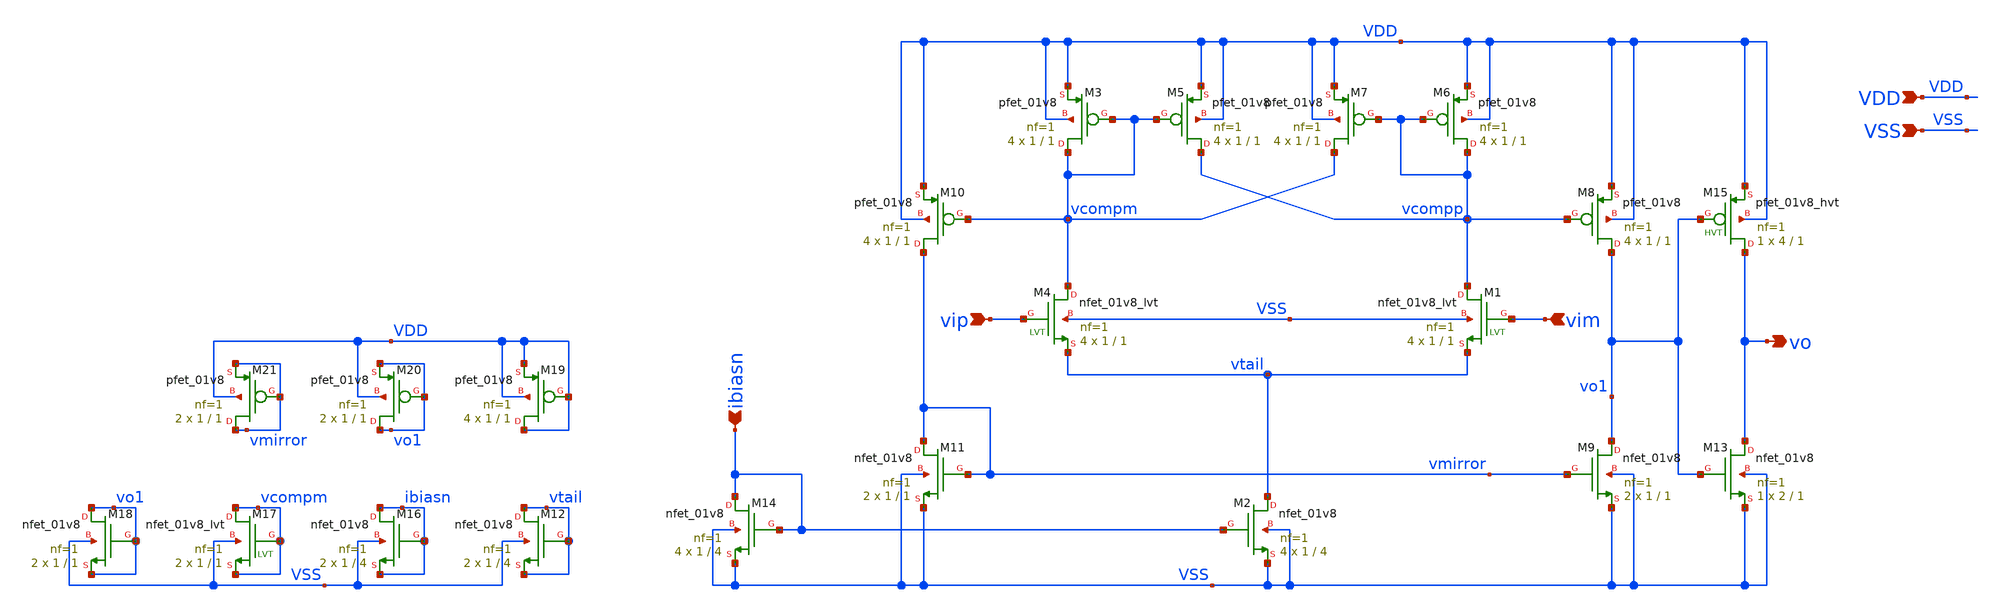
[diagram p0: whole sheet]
** sch_path: designs/comparator_lvs.sch
* Copyright 2020 Stefan Frederik Schippers
* Licensed under the Apache License, Version 2.0 (the "License");
* you may not use this file except in compliance with the License.
* You may obtain a copy of the License at
* https://www.apache.org/licenses/LICENSE-2.0
* Unless required by applicable law or agreed to in writing, software
* distributed under the License is distributed on an "AS IS" BASIS,
* WITHOUT WARRANTIES OR CONDITIONS OF ANY KIND, either express or implied.
* See the License for the specific language governing permissions and
* limitations under the License.
**.subckt comparator_lvs vip vim vo ibiasn VDD VSS
*.ipin vip
*.ipin vim
*.opin vo
*.ipin ibiasn
*.ipin VDD
*.ipin VSS
XM6 vcompp vcompp VDD VDD sky130_fd_pr__pfet_01v8 L=1 W=1 nf=1 ad='int((nf+1)/2) * W/nf * 0.29' as='int((nf+2)/2) * W/nf * 0.29'
+ pd='2*int((nf+1)/2) * (W/nf + 0.29)' ps='2*int((nf+2)/2) * (W/nf + 0.29)' nrd='0.29 / W' nrs='0.29 / W'
+ sa=0 sb=0 sd=0 mult=4 m=4
XM3 vcompm vcompm VDD VDD sky130_fd_pr__pfet_01v8 L=1 W=1 nf=1 ad='int((nf+1)/2) * W/nf * 0.29' as='int((nf+2)/2) * W/nf * 0.29'
+ pd='2*int((nf+1)/2) * (W/nf + 0.29)' ps='2*int((nf+2)/2) * (W/nf + 0.29)' nrd='0.29 / W' nrs='0.29 / W'
+ sa=0 sb=0 sd=0 mult=4 m=4
XM2 vtail ibiasn VSS VSS sky130_fd_pr__nfet_01v8 L=4 W=1 nf=1 ad='int((nf+1)/2) * W/nf * 0.29' as='int((nf+2)/2) * W/nf * 0.29'
+ pd='2*int((nf+1)/2) * (W/nf + 0.29)' ps='2*int((nf+2)/2) * (W/nf + 0.29)' nrd='0.29 / W' nrs='0.29 / W'
+ sa=0 sb=0 sd=0 mult=4 m=4
XM14 ibiasn ibiasn VSS VSS sky130_fd_pr__nfet_01v8 L=4 W=1 nf=1 ad='int((nf+1)/2) * W/nf * 0.29' as='int((nf+2)/2) * W/nf * 0.29'
+ pd='2*int((nf+1)/2) * (W/nf + 0.29)' ps='2*int((nf+2)/2) * (W/nf + 0.29)' nrd='0.29 / W' nrs='0.29 / W'
+ sa=0 sb=0 sd=0 mult=4 m=4
XM4 vcompm vip vtail VSS sky130_fd_pr__nfet_01v8_lvt L=1 W=1 nf=1 ad='int((nf+1)/2) * W/nf * 0.29' as='int((nf+2)/2) * W/nf * 0.29'
+ pd='2*int((nf+1)/2) * (W/nf + 0.29)' ps='2*int((nf+2)/2) * (W/nf + 0.29)' nrd='0.29 / W' nrs='0.29 / W'
+ sa=0 sb=0 sd=0 mult=4 m=4
XM1 vcompp vim vtail VSS sky130_fd_pr__nfet_01v8_lvt L=1 W=1 nf=1 ad='int((nf+1)/2) * W/nf * 0.29' as='int((nf+2)/2) * W/nf * 0.29'
+ pd='2*int((nf+1)/2) * (W/nf + 0.29)' ps='2*int((nf+2)/2) * (W/nf + 0.29)' nrd='0.29 / W' nrs='0.29 / W'
+ sa=0 sb=0 sd=0 mult=4 m=4
XM5 vcompp vcompm VDD VDD sky130_fd_pr__pfet_01v8 L=1 W=1 nf=1 ad='int((nf+1)/2) * W/nf * 0.29' as='int((nf+2)/2) * W/nf * 0.29'
+ pd='2*int((nf+1)/2) * (W/nf + 0.29)' ps='2*int((nf+2)/2) * (W/nf + 0.29)' nrd='0.29 / W' nrs='0.29 / W'
+ sa=0 sb=0 sd=0 mult=4 m=4
XM7 vcompm vcompp VDD VDD sky130_fd_pr__pfet_01v8 L=1 W=1 nf=1 ad='int((nf+1)/2) * W/nf * 0.29' as='int((nf+2)/2) * W/nf * 0.29'
+ pd='2*int((nf+1)/2) * (W/nf + 0.29)' ps='2*int((nf+2)/2) * (W/nf + 0.29)' nrd='0.29 / W' nrs='0.29 / W'
+ sa=0 sb=0 sd=0 mult=4 m=4
XM8 vo1 vcompp VDD VDD sky130_fd_pr__pfet_01v8 L=1 W=1 nf=1 ad='int((nf+1)/2) * W/nf * 0.29' as='int((nf+2)/2) * W/nf * 0.29'
+ pd='2*int((nf+1)/2) * (W/nf + 0.29)' ps='2*int((nf+2)/2) * (W/nf + 0.29)' nrd='0.29 / W' nrs='0.29 / W'
+ sa=0 sb=0 sd=0 mult=4 m=4
XM9 vo1 vmirror VSS VSS sky130_fd_pr__nfet_01v8 L=1 W=1 nf=1 ad='int((nf+1)/2) * W/nf * 0.29' as='int((nf+2)/2) * W/nf * 0.29'
+ pd='2*int((nf+1)/2) * (W/nf + 0.29)' ps='2*int((nf+2)/2) * (W/nf + 0.29)' nrd='0.29 / W' nrs='0.29 / W'
+ sa=0 sb=0 sd=0 mult=2 m=2
XM10 vmirror vcompm VDD VDD sky130_fd_pr__pfet_01v8 L=1 W=1 nf=1 ad='int((nf+1)/2) * W/nf * 0.29' as='int((nf+2)/2) * W/nf * 0.29'
+ pd='2*int((nf+1)/2) * (W/nf + 0.29)' ps='2*int((nf+2)/2) * (W/nf + 0.29)' nrd='0.29 / W' nrs='0.29 / W'
+ sa=0 sb=0 sd=0 mult=4 m=4
XM11 vmirror vmirror VSS VSS sky130_fd_pr__nfet_01v8 L=1 W=1 nf=1 ad='int((nf+1)/2) * W/nf * 0.29' as='int((nf+2)/2) * W/nf * 0.29'
+ pd='2*int((nf+1)/2) * (W/nf + 0.29)' ps='2*int((nf+2)/2) * (W/nf + 0.29)' nrd='0.29 / W' nrs='0.29 / W'
+ sa=0 sb=0 sd=0 mult=2 m=2
XM13 vo vo1 VSS VSS sky130_fd_pr__nfet_01v8 L=1 W=2 nf=1 ad='int((nf+1)/2) * W/nf * 0.29' as='int((nf+2)/2) * W/nf * 0.29'
+ pd='2*int((nf+1)/2) * (W/nf + 0.29)' ps='2*int((nf+2)/2) * (W/nf + 0.29)' nrd='0.29 / W' nrs='0.29 / W'
+ sa=0 sb=0 sd=0 mult=1 m=1
XM15 vo vo1 VDD VDD sky130_fd_pr__pfet_01v8_hvt L=1 W=4 nf=1 ad='int((nf+1)/2) * W/nf * 0.29' as='int((nf+2)/2) * W/nf * 0.29'
+ pd='2*int((nf+1)/2) * (W/nf + 0.29)' ps='2*int((nf+2)/2) * (W/nf + 0.29)' nrd='0.29 / W' nrs='0.29 / W'
+ sa=0 sb=0 sd=0 mult=1 m=1
XM12 vtail vtail vtail VSS sky130_fd_pr__nfet_01v8 L=4 W=1 nf=1 ad='int((nf+1)/2) * W/nf * 0.29' as='int((nf+2)/2) * W/nf * 0.29'
+ pd='2*int((nf+1)/2) * (W/nf + 0.29)' ps='2*int((nf+2)/2) * (W/nf + 0.29)' nrd='0.29 / W' nrs='0.29 / W'
+ sa=0 sb=0 sd=0 mult=2 m=2
XM16 ibiasn ibiasn ibiasn VSS sky130_fd_pr__nfet_01v8 L=4 W=1 nf=1 ad='int((nf+1)/2) * W/nf * 0.29' as='int((nf+2)/2) * W/nf * 0.29'
+ pd='2*int((nf+1)/2) * (W/nf + 0.29)' ps='2*int((nf+2)/2) * (W/nf + 0.29)' nrd='0.29 / W' nrs='0.29 / W'
+ sa=0 sb=0 sd=0 mult=2 m=2
XM18 vo1 vo1 vo1 VSS sky130_fd_pr__nfet_01v8 L=1 W=1 nf=1 ad='int((nf+1)/2) * W/nf * 0.29' as='int((nf+2)/2) * W/nf * 0.29'
+ pd='2*int((nf+1)/2) * (W/nf + 0.29)' ps='2*int((nf+2)/2) * (W/nf + 0.29)' nrd='0.29 / W' nrs='0.29 / W'
+ sa=0 sb=0 sd=0 mult=2 m=2
XM19 VDD VDD VDD VDD sky130_fd_pr__pfet_01v8 L=1 W=1 nf=1 ad='int((nf+1)/2) * W/nf * 0.29' as='int((nf+2)/2) * W/nf * 0.29'
+ pd='2*int((nf+1)/2) * (W/nf + 0.29)' ps='2*int((nf+2)/2) * (W/nf + 0.29)' nrd='0.29 / W' nrs='0.29 / W'
+ sa=0 sb=0 sd=0 mult=4 m=4
XM20 vo1 vo1 vo1 VDD sky130_fd_pr__pfet_01v8 L=1 W=1 nf=1 ad='int((nf+1)/2) * W/nf * 0.29' as='int((nf+2)/2) * W/nf * 0.29'
+ pd='2*int((nf+1)/2) * (W/nf + 0.29)' ps='2*int((nf+2)/2) * (W/nf + 0.29)' nrd='0.29 / W' nrs='0.29 / W'
+ sa=0 sb=0 sd=0 mult=2 m=2
XM21 vmirror vmirror vmirror VDD sky130_fd_pr__pfet_01v8 L=1 W=1 nf=1 ad='int((nf+1)/2) * W/nf * 0.29'
+ as='int((nf+2)/2) * W/nf * 0.29' pd='2*int((nf+1)/2) * (W/nf + 0.29)' ps='2*int((nf+2)/2) * (W/nf + 0.29)'
+ nrd='0.29 / W' nrs='0.29 / W' sa=0 sb=0 sd=0 mult=2 m=2
XM17 vcompm vcompm vcompm VSS sky130_fd_pr__nfet_01v8_lvt L=1 W=1 nf=1 ad='int((nf+1)/2) * W/nf * 0.29'
+ as='int((nf+2)/2) * W/nf * 0.29' pd='2*int((nf+1)/2) * (W/nf + 0.29)' ps='2*int((nf+2)/2) * (W/nf + 0.29)'
+ nrd='0.29 / W' nrs='0.29 / W' sa=0 sb=0 sd=0 mult=2 m=2
**.ends
.end
